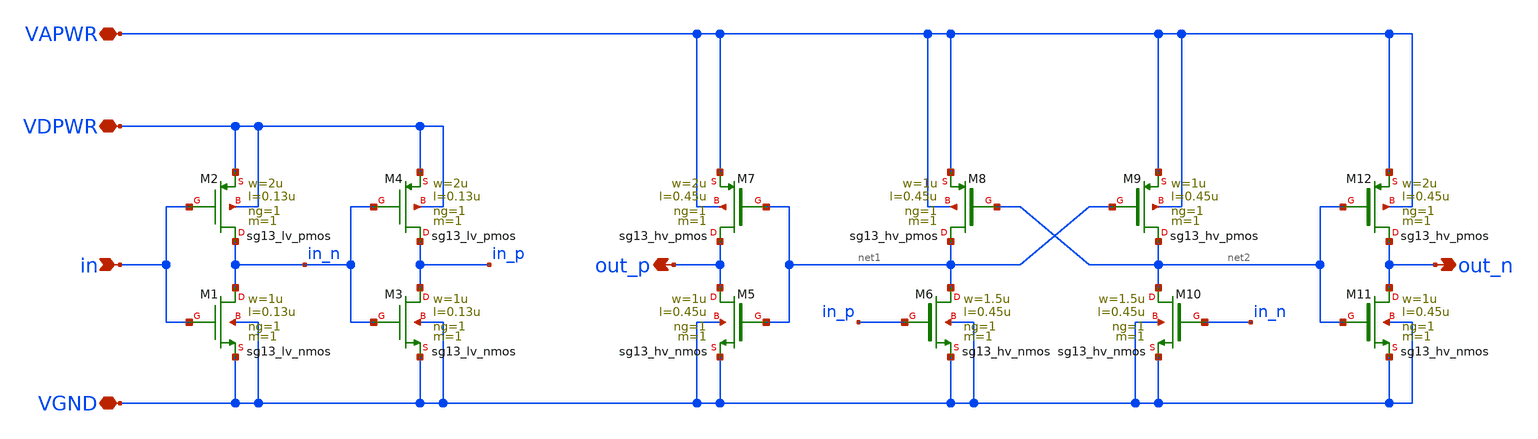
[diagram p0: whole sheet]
** sch_path: ihp-sg13cmos5l/libs.tech/xschem/hm_analog/lv2hv.sch
**.subckt lv2hv VAPWR VGND in VDPWR out_p out_n
*.iopin VAPWR
*.iopin VGND
*.ipin in
*.iopin VDPWR
*.opin out_p
*.opin out_n
XM1 in_n in VGND VGND sg13_lv_nmos w=1u l=0.13u ng=1 m=1 mm_ok=1
XM2 in_n in VDPWR VDPWR sg13_lv_pmos w=2u l=0.13u ng=1 m=1 mm_ok=1
XM3 in_p in_n VGND VGND sg13_lv_nmos w=1u l=0.13u ng=1 m=1 mm_ok=1
XM4 in_p in_n VDPWR VDPWR sg13_lv_pmos w=2u l=0.13u ng=1 m=1 mm_ok=1
XM5 out_p net1 VGND VGND sg13_hv_nmos w=1u l=0.45u ng=1 m=1 mm_ok=1
XM6 net1 in_p VGND VGND sg13_hv_nmos w=1.5u l=0.45u ng=1 m=1 mm_ok=1
XM7 out_p net1 VAPWR VAPWR sg13_hv_pmos w=2u l=0.45u ng=1 m=1 mm_ok=1
XM8 net1 net2 VAPWR VAPWR sg13_hv_pmos w=1u l=0.45u ng=1 m=1 mm_ok=1
XM9 net2 net1 VAPWR VAPWR sg13_hv_pmos w=1u l=0.45u ng=1 m=1 mm_ok=1
XM10 net2 in_n VGND VGND sg13_hv_nmos w=1.5u l=0.45u ng=1 m=1 mm_ok=1
XM11 out_n net2 VGND VGND sg13_hv_nmos w=1u l=0.45u ng=1 m=1 mm_ok=1
XM12 out_n net2 VAPWR VAPWR sg13_hv_pmos w=2u l=0.45u ng=1 m=1 mm_ok=1
**.ends
.end
